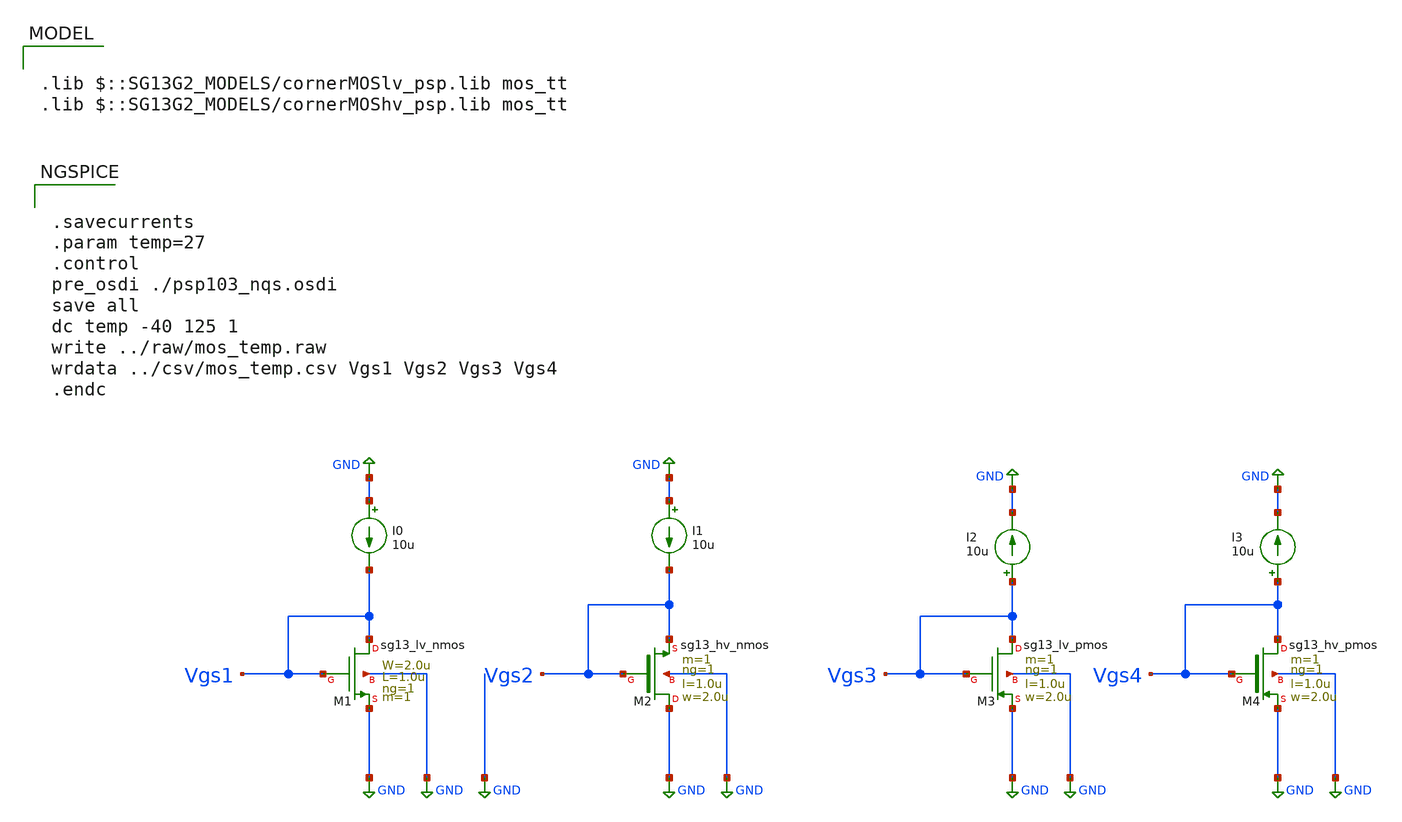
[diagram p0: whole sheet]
** sch_path: ihp-sg13g2/libs.tech/xschem/sg13g2_tests/dc_mos_cs_temp.sch
* Copyright 2023 IHP PDK Authors
**.subckt dc_mos_cs_temp
XM1 Vgs1 Vgs1 GND GND sg13_lv_nmos W=2.0u L=1.0u ng=1 m=1
XM2 GND Vgs2 Vgs2 GND sg13_hv_nmos w=2.0u l=1.0u ng=1 m=1 mm_ok=1
XM3 Vgs3 Vgs3 GND GND sg13_lv_pmos w=2.0u l=1.0u ng=1 m=1 mm_ok=1
XM4 Vgs4 Vgs4 GND GND sg13_hv_pmos w=2.0u l=1.0u ng=1 m=1 mm_ok=1
I0 GND Vgs1 10u
I1 GND Vgs2 10u
I2 Vgs3 GND 10u
I3 Vgs4 GND 10u
**** begin user architecture code

.lib $::SG13G2_MODELS/cornerMOSlv_psp.lib mos_tt
.lib $::SG13G2_MODELS/cornerMOShv_psp.lib mos_tt



.savecurrents
.param temp=27
.control
pre_osdi ./psp103_nqs.osdi
save all
dc temp -40 125 1
write ../raw/mos_temp.raw
wrdata ../csv/mos_temp.csv Vgs1 Vgs2 Vgs3 Vgs4
.endc


**** end user architecture code
**.ends
.GLOBAL GND
.end
